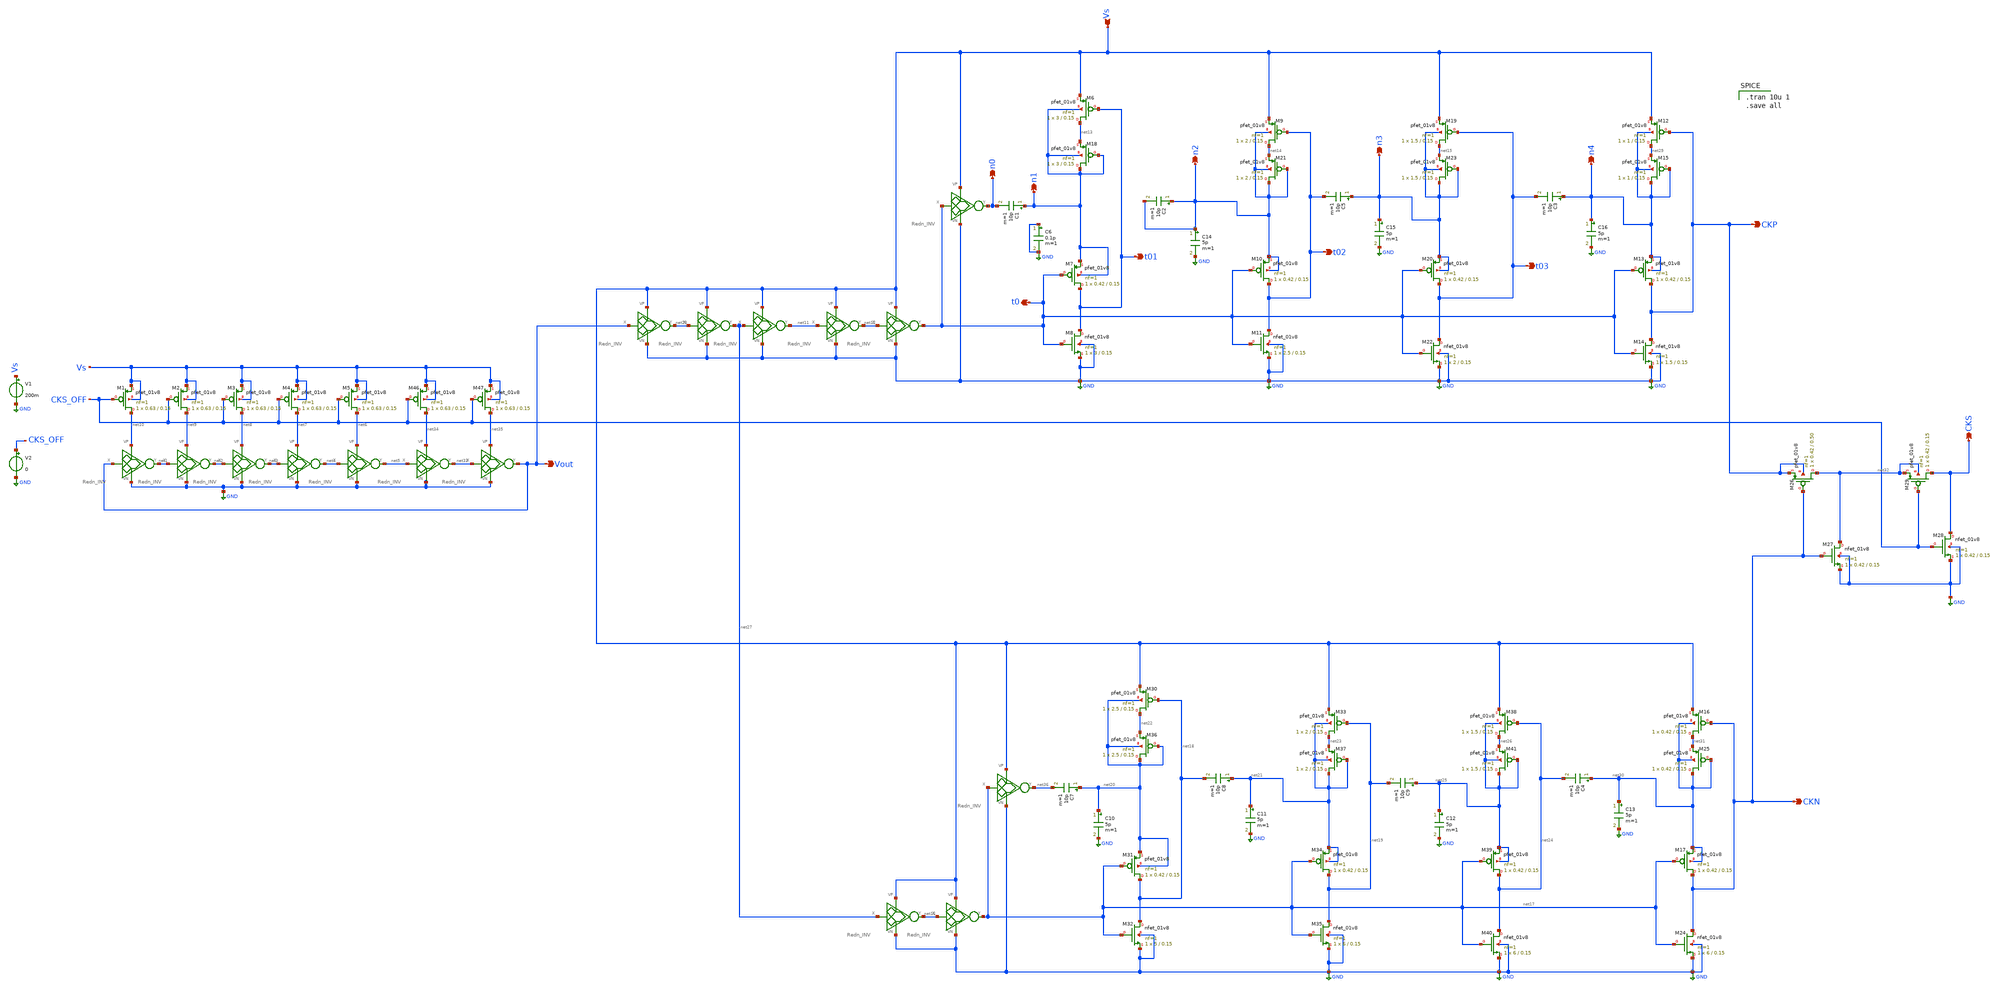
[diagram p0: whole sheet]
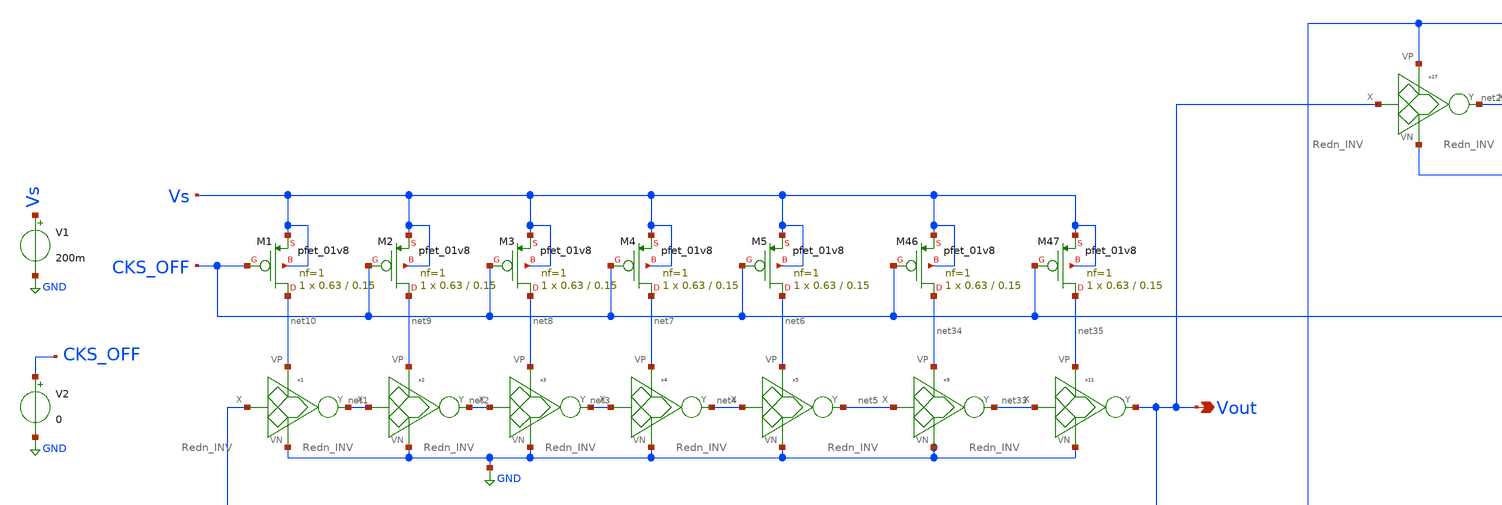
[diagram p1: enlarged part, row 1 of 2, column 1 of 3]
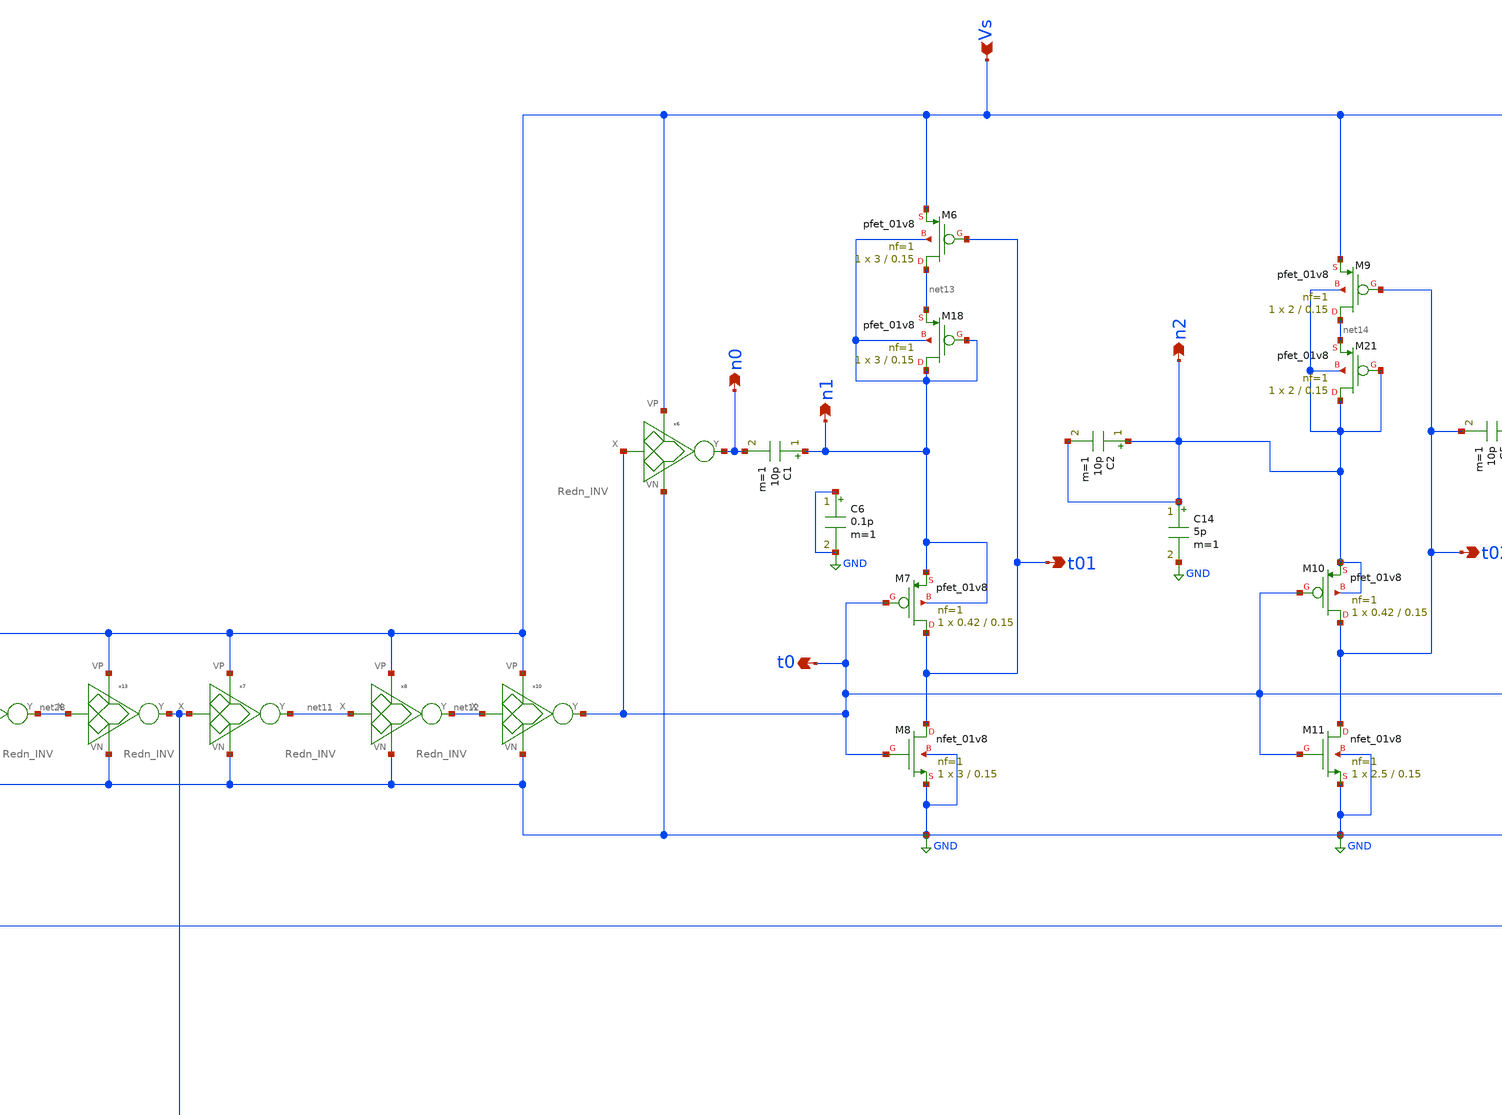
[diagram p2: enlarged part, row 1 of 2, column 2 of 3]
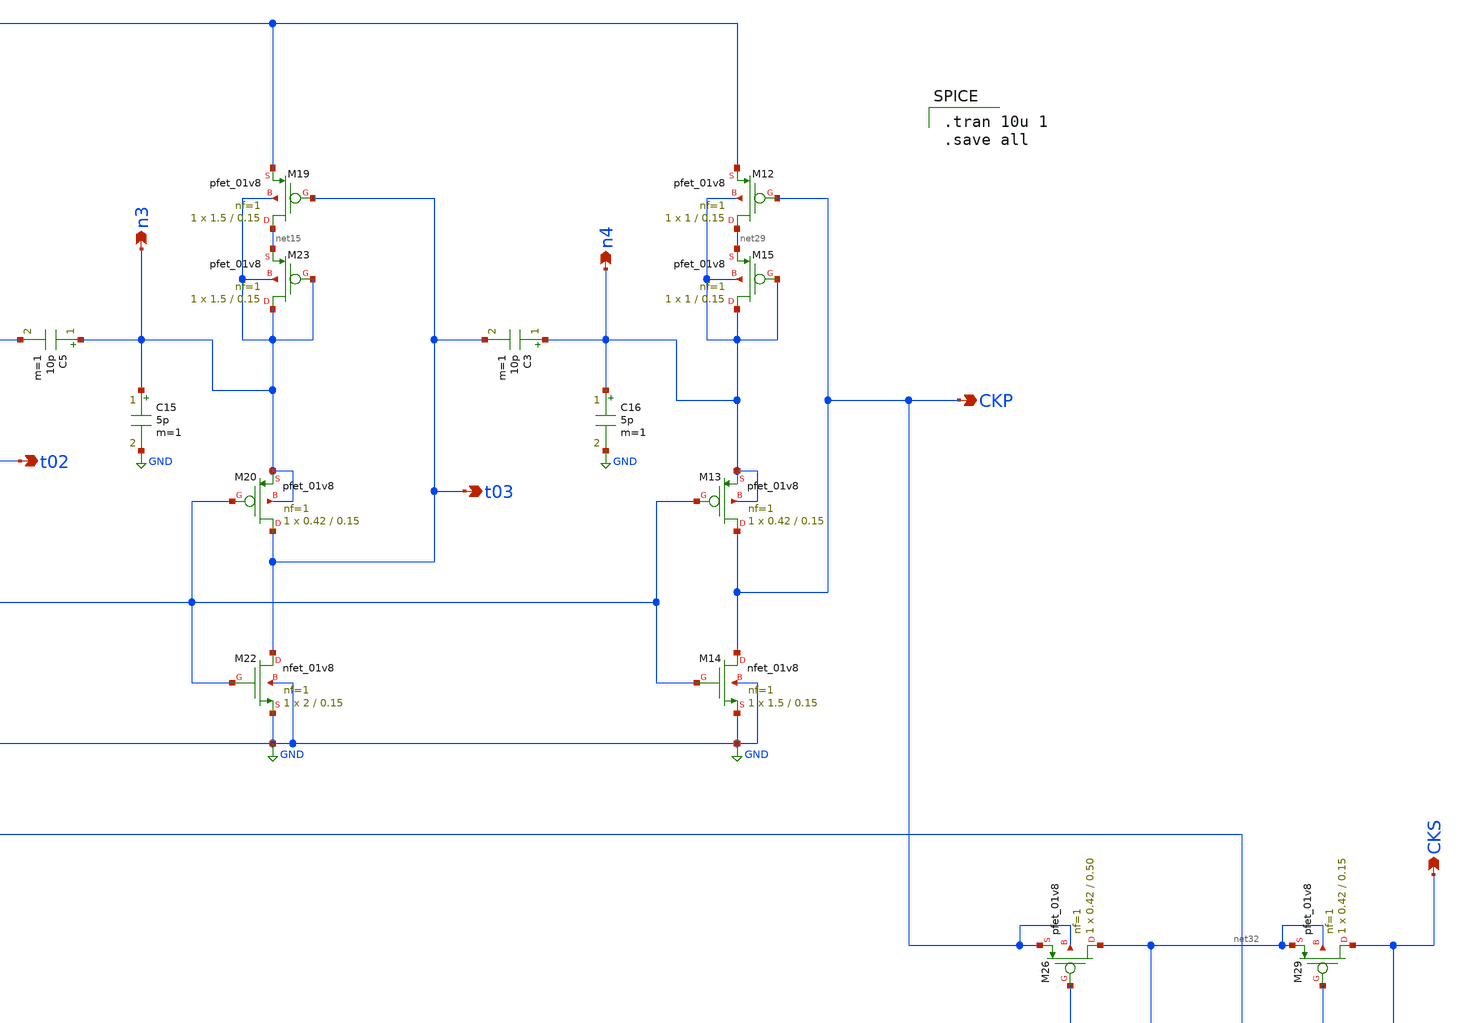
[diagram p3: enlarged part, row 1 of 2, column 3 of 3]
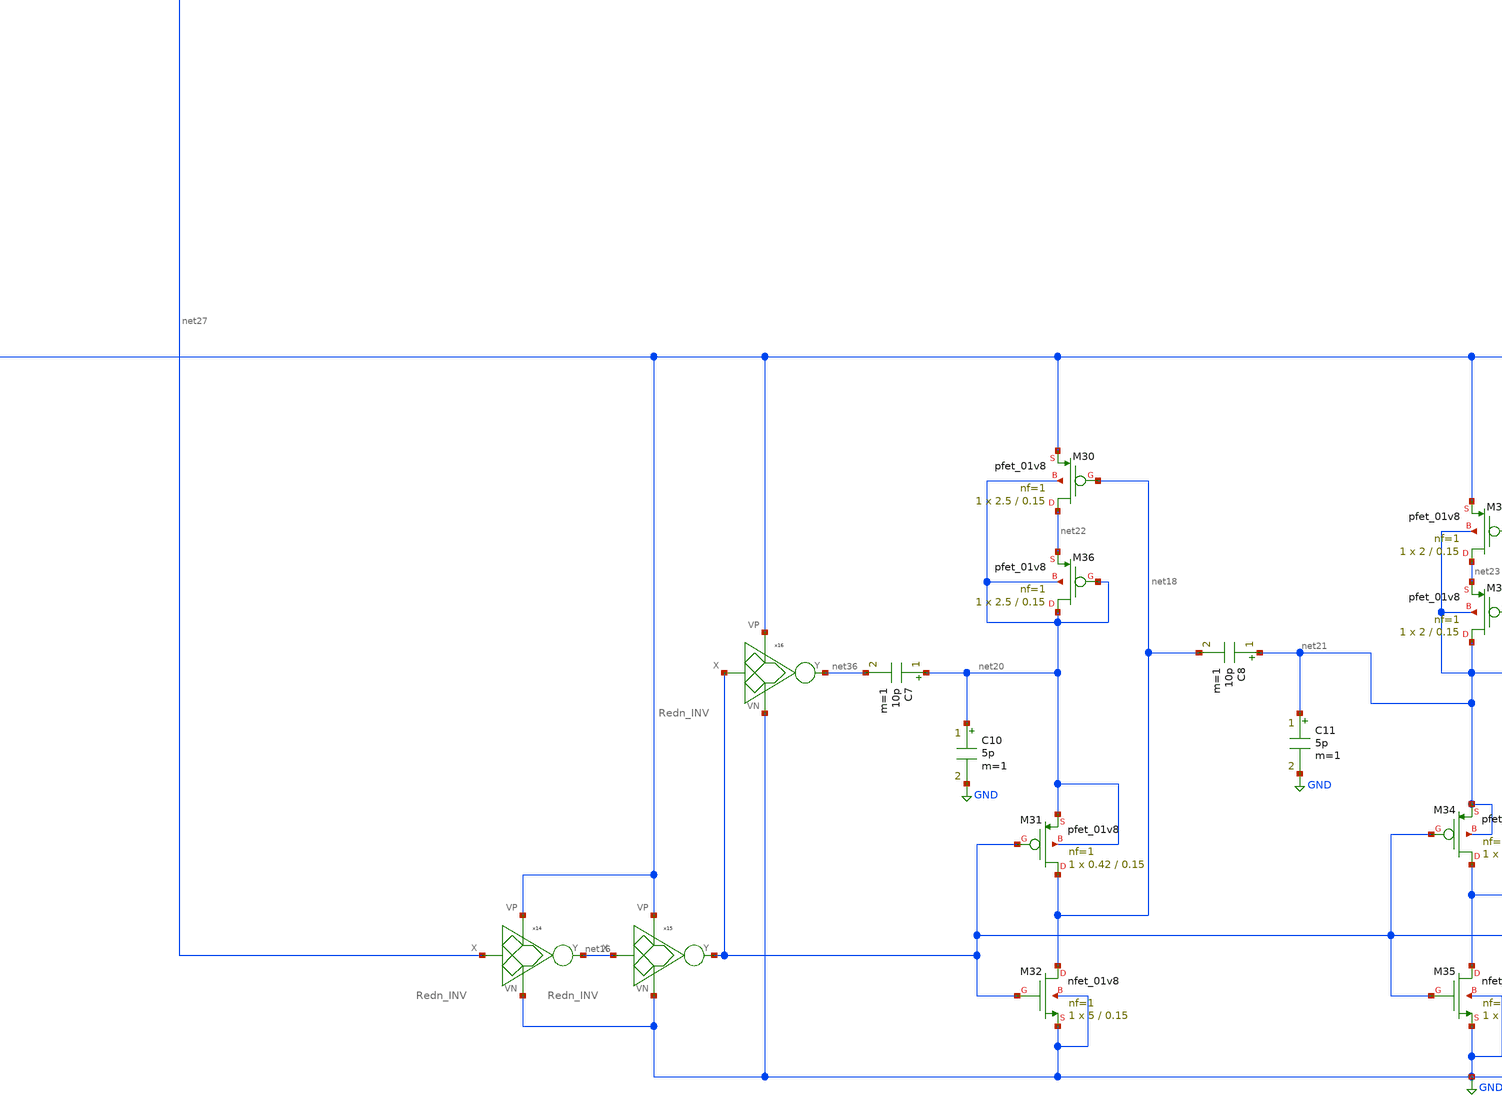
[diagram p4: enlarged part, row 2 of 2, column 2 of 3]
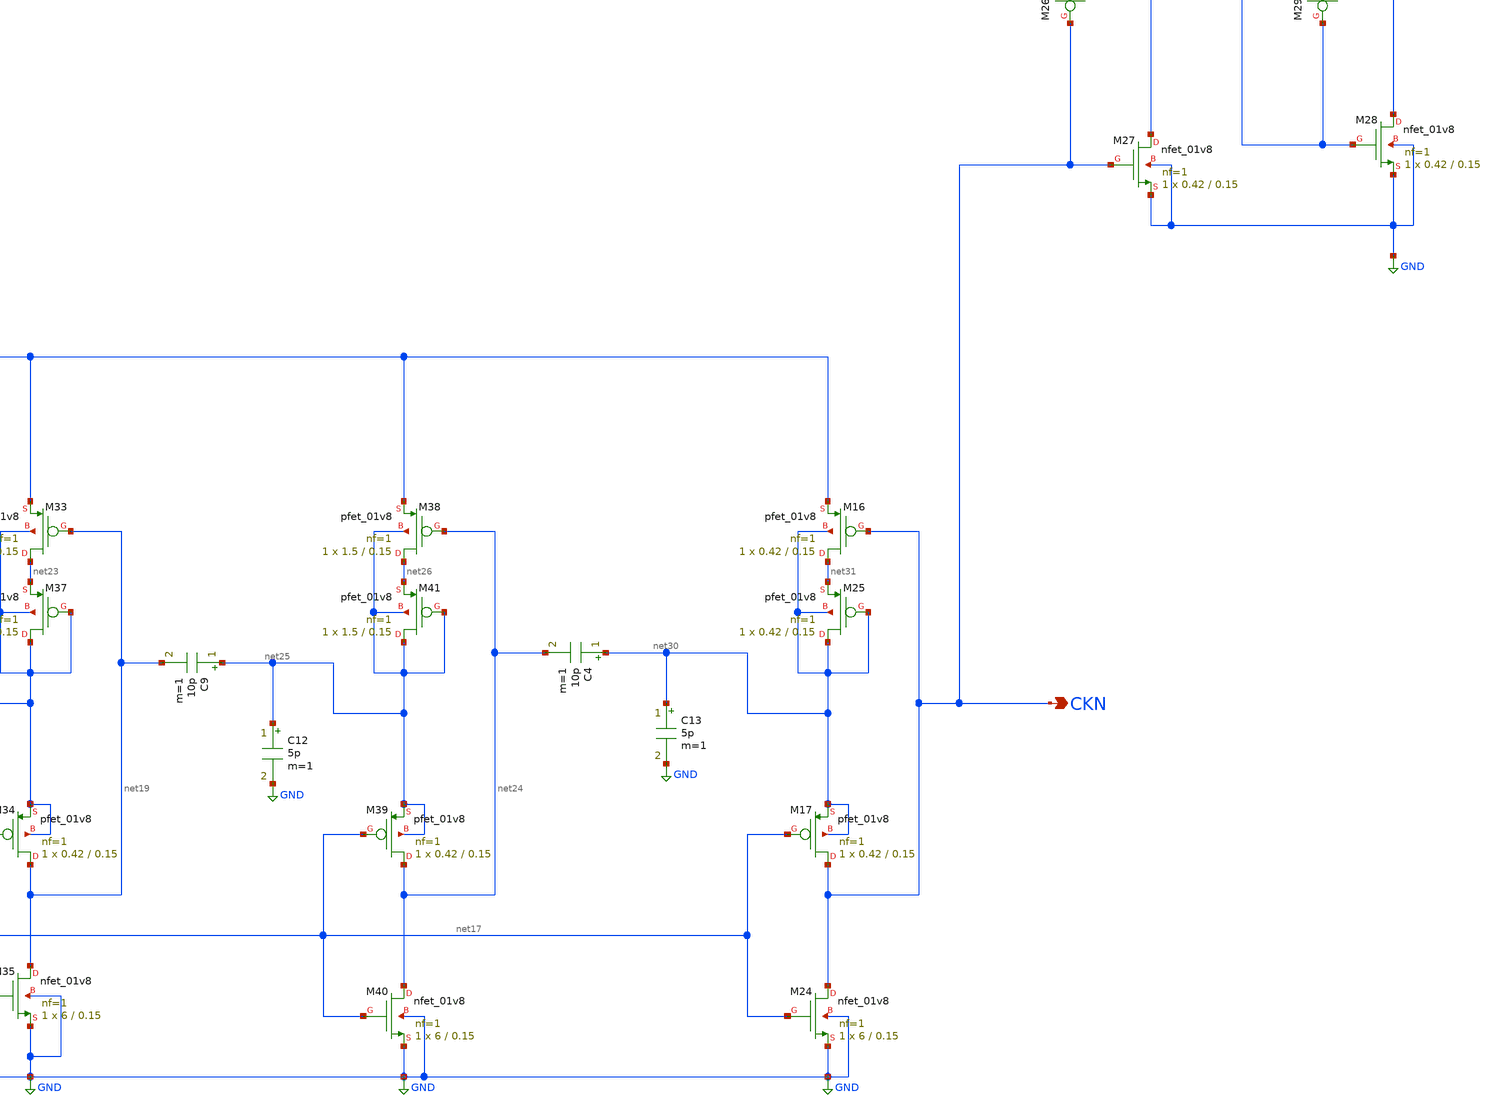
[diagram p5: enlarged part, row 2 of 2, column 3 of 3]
** sch_path: Blocks/Startup Converter/Startup_Conv_3.sch
**.subckt Startup_Conv_3 Vout Vs t02 CKP CKN CKS t03 t01 t0 n1 n2 n3 n4 n0
*.opin Vout
*.ipin Vs
*.opin t02
*.opin CKP
*.opin CKN
*.opin CKS
*.opin t03
*.opin t01
*.opin t0
*.opin n1
*.opin n2
*.opin n3
*.opin n4
*.opin n0
V1 Vs GND 200m
XM1 net10 CKS_OFF Vs Vs sky130_fd_pr__pfet_01v8 L=0.15 W=0.63 nf=1 ad='int((nf+1)/2) * W/nf * 0.29' as='int((nf+2)/2) * W/nf * 0.29'
+ pd='2*int((nf+1)/2) * (W/nf + 0.29)' ps='2*int((nf+2)/2) * (W/nf + 0.29)' nrd='0.29 / W' nrs='0.29 / W'
+ sa=0 sb=0 sd=0 mult=1 m=1
XM2 net9 CKS_OFF Vs Vs sky130_fd_pr__pfet_01v8 L=0.15 W=0.63 nf=1 ad='int((nf+1)/2) * W/nf * 0.29' as='int((nf+2)/2) * W/nf * 0.29'
+ pd='2*int((nf+1)/2) * (W/nf + 0.29)' ps='2*int((nf+2)/2) * (W/nf + 0.29)' nrd='0.29 / W' nrs='0.29 / W'
+ sa=0 sb=0 sd=0 mult=1 m=1
XM3 net8 CKS_OFF Vs Vs sky130_fd_pr__pfet_01v8 L=0.15 W=0.63 nf=1 ad='int((nf+1)/2) * W/nf * 0.29' as='int((nf+2)/2) * W/nf * 0.29'
+ pd='2*int((nf+1)/2) * (W/nf + 0.29)' ps='2*int((nf+2)/2) * (W/nf + 0.29)' nrd='0.29 / W' nrs='0.29 / W'
+ sa=0 sb=0 sd=0 mult=1 m=1
XM4 net7 CKS_OFF Vs Vs sky130_fd_pr__pfet_01v8 L=0.15 W=0.63 nf=1 ad='int((nf+1)/2) * W/nf * 0.29' as='int((nf+2)/2) * W/nf * 0.29'
+ pd='2*int((nf+1)/2) * (W/nf + 0.29)' ps='2*int((nf+2)/2) * (W/nf + 0.29)' nrd='0.29 / W' nrs='0.29 / W'
+ sa=0 sb=0 sd=0 mult=1 m=1
XM5 net6 CKS_OFF Vs Vs sky130_fd_pr__pfet_01v8 L=0.15 W=0.63 nf=1 ad='int((nf+1)/2) * W/nf * 0.29' as='int((nf+2)/2) * W/nf * 0.29'
+ pd='2*int((nf+1)/2) * (W/nf + 0.29)' ps='2*int((nf+2)/2) * (W/nf + 0.29)' nrd='0.29 / W' nrs='0.29 / W'
+ sa=0 sb=0 sd=0 mult=1 m=1
V2 CKS_OFF GND 0
x1 Vout net1 net10 GND Redn_INV
x2 net1 net2 net9 GND Redn_INV
x3 net2 net3 net8 GND Redn_INV
x4 net3 net4 net7 GND Redn_INV
x5 net4 net5 net6 GND Redn_INV
C1 n1 n0 10p m=1
XM6 net13 t01 Vs n1 sky130_fd_pr__pfet_01v8 L=0.15 W=3 nf=1 ad='int((nf+1)/2) * W/nf * 0.29' as='int((nf+2)/2) * W/nf * 0.29'
+ pd='2*int((nf+1)/2) * (W/nf + 0.29)' ps='2*int((nf+2)/2) * (W/nf + 0.29)' nrd='0.29 / W' nrs='0.29 / W'
+ sa=0 sb=0 sd=0 mult=1 m=1
XM9 net14 t02 Vs n2 sky130_fd_pr__pfet_01v8 L=0.15 W=2 nf=1 ad='int((nf+1)/2) * W/nf * 0.29' as='int((nf+2)/2) * W/nf * 0.29'
+ pd='2*int((nf+1)/2) * (W/nf + 0.29)' ps='2*int((nf+2)/2) * (W/nf + 0.29)' nrd='0.29 / W' nrs='0.29 / W'
+ sa=0 sb=0 sd=0 mult=1 m=1
XM10 t02 t0 n2 n2 sky130_fd_pr__pfet_01v8 L=0.15 W=0.42 nf=1 ad='int((nf+1)/2) * W/nf * 0.29' as='int((nf+2)/2) * W/nf * 0.29'
+ pd='2*int((nf+1)/2) * (W/nf + 0.29)' ps='2*int((nf+2)/2) * (W/nf + 0.29)' nrd='0.29 / W' nrs='0.29 / W'
+ sa=0 sb=0 sd=0 mult=1 m=1
XM11 t02 t0 GND GND sky130_fd_pr__nfet_01v8 L=0.15 W=2.5 nf=1 ad='int((nf+1)/2) * W/nf * 0.29' as='int((nf+2)/2) * W/nf * 0.29'
+ pd='2*int((nf+1)/2) * (W/nf + 0.29)' ps='2*int((nf+2)/2) * (W/nf + 0.29)' nrd='0.29 / W' nrs='0.29 / W'
+ sa=0 sb=0 sd=0 mult=1 m=1
XM18 n1 n1 net13 n1 sky130_fd_pr__pfet_01v8 L=0.15 W=3 nf=1 ad='int((nf+1)/2) * W/nf * 0.29' as='int((nf+2)/2) * W/nf * 0.29'
+ pd='2*int((nf+1)/2) * (W/nf + 0.29)' ps='2*int((nf+2)/2) * (W/nf + 0.29)' nrd='0.29 / W' nrs='0.29 / W'
+ sa=0 sb=0 sd=0 mult=1 m=1
XM21 n2 n2 net14 n2 sky130_fd_pr__pfet_01v8 L=0.15 W=2 nf=1 ad='int((nf+1)/2) * W/nf * 0.29' as='int((nf+2)/2) * W/nf * 0.29'
+ pd='2*int((nf+1)/2) * (W/nf + 0.29)' ps='2*int((nf+2)/2) * (W/nf + 0.29)' nrd='0.29 / W' nrs='0.29 / W'
+ sa=0 sb=0 sd=0 mult=1 m=1
C2 n2 n2 10p m=1
x7 net27 net11 Vs GND Redn_INV
x8 net11 net12 Vs GND Redn_INV
x10 net12 t0 Vs GND Redn_INV
x6 t0 n0 Vs GND Redn_INV
XM19 net15 t03 Vs n3 sky130_fd_pr__pfet_01v8 L=0.15 W=1.5 nf=1 ad='int((nf+1)/2) * W/nf * 0.29' as='int((nf+2)/2) * W/nf * 0.29'
+ pd='2*int((nf+1)/2) * (W/nf + 0.29)' ps='2*int((nf+2)/2) * (W/nf + 0.29)' nrd='0.29 / W' nrs='0.29 / W'
+ sa=0 sb=0 sd=0 mult=1 m=1
XM20 t03 t0 n3 n3 sky130_fd_pr__pfet_01v8 L=0.15 W=0.42 nf=1 ad='int((nf+1)/2) * W/nf * 0.29' as='int((nf+2)/2) * W/nf * 0.29'
+ pd='2*int((nf+1)/2) * (W/nf + 0.29)' ps='2*int((nf+2)/2) * (W/nf + 0.29)' nrd='0.29 / W' nrs='0.29 / W'
+ sa=0 sb=0 sd=0 mult=1 m=1
XM22 t03 t0 GND GND sky130_fd_pr__nfet_01v8 L=0.15 W=2 nf=1 ad='int((nf+1)/2) * W/nf * 0.29' as='int((nf+2)/2) * W/nf * 0.29'
+ pd='2*int((nf+1)/2) * (W/nf + 0.29)' ps='2*int((nf+2)/2) * (W/nf + 0.29)' nrd='0.29 / W' nrs='0.29 / W'
+ sa=0 sb=0 sd=0 mult=1 m=1
XM23 n3 n3 net15 n3 sky130_fd_pr__pfet_01v8 L=0.15 W=1.5 nf=1 ad='int((nf+1)/2) * W/nf * 0.29' as='int((nf+2)/2) * W/nf * 0.29'
+ pd='2*int((nf+1)/2) * (W/nf + 0.29)' ps='2*int((nf+2)/2) * (W/nf + 0.29)' nrd='0.29 / W' nrs='0.29 / W'
+ sa=0 sb=0 sd=0 mult=1 m=1
C5 n3 t02 10p m=1
C7 net20 net36 10p m=1
XM30 net22 net18 Vs net20 sky130_fd_pr__pfet_01v8 L=0.15 W=2.5 nf=1 ad='int((nf+1)/2) * W/nf * 0.29'
+ as='int((nf+2)/2) * W/nf * 0.29' pd='2*int((nf+1)/2) * (W/nf + 0.29)' ps='2*int((nf+2)/2) * (W/nf + 0.29)'
+ nrd='0.29 / W' nrs='0.29 / W' sa=0 sb=0 sd=0 mult=1 m=1
XM31 net18 net17 net20 net20 sky130_fd_pr__pfet_01v8 L=0.15 W=0.42 nf=1 ad='int((nf+1)/2) * W/nf * 0.29'
+ as='int((nf+2)/2) * W/nf * 0.29' pd='2*int((nf+1)/2) * (W/nf + 0.29)' ps='2*int((nf+2)/2) * (W/nf + 0.29)'
+ nrd='0.29 / W' nrs='0.29 / W' sa=0 sb=0 sd=0 mult=1 m=1
XM32 net18 net17 GND GND sky130_fd_pr__nfet_01v8 L=0.15 W=5 nf=1 ad='int((nf+1)/2) * W/nf * 0.29' as='int((nf+2)/2) * W/nf * 0.29'
+ pd='2*int((nf+1)/2) * (W/nf + 0.29)' ps='2*int((nf+2)/2) * (W/nf + 0.29)' nrd='0.29 / W' nrs='0.29 / W'
+ sa=0 sb=0 sd=0 mult=1 m=1
XM33 net23 net19 Vs net21 sky130_fd_pr__pfet_01v8 L=0.15 W=2 nf=1 ad='int((nf+1)/2) * W/nf * 0.29' as='int((nf+2)/2) * W/nf * 0.29'
+ pd='2*int((nf+1)/2) * (W/nf + 0.29)' ps='2*int((nf+2)/2) * (W/nf + 0.29)' nrd='0.29 / W' nrs='0.29 / W'
+ sa=0 sb=0 sd=0 mult=1 m=1
XM34 net19 net17 net21 net21 sky130_fd_pr__pfet_01v8 L=0.15 W=0.42 nf=1 ad='int((nf+1)/2) * W/nf * 0.29'
+ as='int((nf+2)/2) * W/nf * 0.29' pd='2*int((nf+1)/2) * (W/nf + 0.29)' ps='2*int((nf+2)/2) * (W/nf + 0.29)'
+ nrd='0.29 / W' nrs='0.29 / W' sa=0 sb=0 sd=0 mult=1 m=1
XM35 net19 net17 GND GND sky130_fd_pr__nfet_01v8 L=0.15 W=6 nf=1 ad='int((nf+1)/2) * W/nf * 0.29' as='int((nf+2)/2) * W/nf * 0.29'
+ pd='2*int((nf+1)/2) * (W/nf + 0.29)' ps='2*int((nf+2)/2) * (W/nf + 0.29)' nrd='0.29 / W' nrs='0.29 / W'
+ sa=0 sb=0 sd=0 mult=1 m=1
XM36 net20 net20 net22 net20 sky130_fd_pr__pfet_01v8 L=0.15 W=2.5 nf=1 ad='int((nf+1)/2) * W/nf * 0.29'
+ as='int((nf+2)/2) * W/nf * 0.29' pd='2*int((nf+1)/2) * (W/nf + 0.29)' ps='2*int((nf+2)/2) * (W/nf + 0.29)'
+ nrd='0.29 / W' nrs='0.29 / W' sa=0 sb=0 sd=0 mult=1 m=1
XM37 net21 net21 net23 net21 sky130_fd_pr__pfet_01v8 L=0.15 W=2 nf=1 ad='int((nf+1)/2) * W/nf * 0.29'
+ as='int((nf+2)/2) * W/nf * 0.29' pd='2*int((nf+1)/2) * (W/nf + 0.29)' ps='2*int((nf+2)/2) * (W/nf + 0.29)'
+ nrd='0.29 / W' nrs='0.29 / W' sa=0 sb=0 sd=0 mult=1 m=1
C8 net21 net18 10p m=1
x14 net27 net16 Vs GND Redn_INV
x15 net16 net17 Vs GND Redn_INV
x16 net17 net36 Vs GND Redn_INV
XM38 net26 net24 Vs net25 sky130_fd_pr__pfet_01v8 L=0.15 W=1.5 nf=1 ad='int((nf+1)/2) * W/nf * 0.29'
+ as='int((nf+2)/2) * W/nf * 0.29' pd='2*int((nf+1)/2) * (W/nf + 0.29)' ps='2*int((nf+2)/2) * (W/nf + 0.29)'
+ nrd='0.29 / W' nrs='0.29 / W' sa=0 sb=0 sd=0 mult=1 m=1
XM39 net24 net17 net25 net25 sky130_fd_pr__pfet_01v8 L=0.15 W=0.42 nf=1 ad='int((nf+1)/2) * W/nf * 0.29'
+ as='int((nf+2)/2) * W/nf * 0.29' pd='2*int((nf+1)/2) * (W/nf + 0.29)' ps='2*int((nf+2)/2) * (W/nf + 0.29)'
+ nrd='0.29 / W' nrs='0.29 / W' sa=0 sb=0 sd=0 mult=1 m=1
XM40 net24 net17 GND GND sky130_fd_pr__nfet_01v8 L=0.15 W=6 nf=1 ad='int((nf+1)/2) * W/nf * 0.29' as='int((nf+2)/2) * W/nf * 0.29'
+ pd='2*int((nf+1)/2) * (W/nf + 0.29)' ps='2*int((nf+2)/2) * (W/nf + 0.29)' nrd='0.29 / W' nrs='0.29 / W'
+ sa=0 sb=0 sd=0 mult=1 m=1
XM41 net25 net25 net26 net25 sky130_fd_pr__pfet_01v8 L=0.15 W=1.5 nf=1 ad='int((nf+1)/2) * W/nf * 0.29'
+ as='int((nf+2)/2) * W/nf * 0.29' pd='2*int((nf+1)/2) * (W/nf + 0.29)' ps='2*int((nf+2)/2) * (W/nf + 0.29)'
+ nrd='0.29 / W' nrs='0.29 / W' sa=0 sb=0 sd=0 mult=1 m=1
C9 net25 net19 10p m=1
x13 net28 net27 Vs GND Redn_INV
x17 Vout net28 Vs GND Redn_INV
XM12 net29 CKP Vs n4 sky130_fd_pr__pfet_01v8 L=0.15 W=1 nf=1 ad='int((nf+1)/2) * W/nf * 0.29' as='int((nf+2)/2) * W/nf * 0.29'
+ pd='2*int((nf+1)/2) * (W/nf + 0.29)' ps='2*int((nf+2)/2) * (W/nf + 0.29)' nrd='0.29 / W' nrs='0.29 / W'
+ sa=0 sb=0 sd=0 mult=1 m=1
XM13 CKP t0 n4 n4 sky130_fd_pr__pfet_01v8 L=0.15 W=0.42 nf=1 ad='int((nf+1)/2) * W/nf * 0.29' as='int((nf+2)/2) * W/nf * 0.29'
+ pd='2*int((nf+1)/2) * (W/nf + 0.29)' ps='2*int((nf+2)/2) * (W/nf + 0.29)' nrd='0.29 / W' nrs='0.29 / W'
+ sa=0 sb=0 sd=0 mult=1 m=1
XM14 CKP t0 GND GND sky130_fd_pr__nfet_01v8 L=0.15 W=1.5 nf=1 ad='int((nf+1)/2) * W/nf * 0.29' as='int((nf+2)/2) * W/nf * 0.29'
+ pd='2*int((nf+1)/2) * (W/nf + 0.29)' ps='2*int((nf+2)/2) * (W/nf + 0.29)' nrd='0.29 / W' nrs='0.29 / W'
+ sa=0 sb=0 sd=0 mult=1 m=1
XM15 n4 n4 net29 n4 sky130_fd_pr__pfet_01v8 L=0.15 W=1 nf=1 ad='int((nf+1)/2) * W/nf * 0.29' as='int((nf+2)/2) * W/nf * 0.29'
+ pd='2*int((nf+1)/2) * (W/nf + 0.29)' ps='2*int((nf+2)/2) * (W/nf + 0.29)' nrd='0.29 / W' nrs='0.29 / W'
+ sa=0 sb=0 sd=0 mult=1 m=1
C3 n4 t03 10p m=1
XM16 net31 CKN Vs net30 sky130_fd_pr__pfet_01v8 L=0.15 W=0.42 nf=1 ad='int((nf+1)/2) * W/nf * 0.29' as='int((nf+2)/2) * W/nf * 0.29'
+ pd='2*int((nf+1)/2) * (W/nf + 0.29)' ps='2*int((nf+2)/2) * (W/nf + 0.29)' nrd='0.29 / W' nrs='0.29 / W'
+ sa=0 sb=0 sd=0 mult=1 m=1
XM17 CKN net17 net30 net30 sky130_fd_pr__pfet_01v8 L=0.15 W=0.42 nf=1 ad='int((nf+1)/2) * W/nf * 0.29'
+ as='int((nf+2)/2) * W/nf * 0.29' pd='2*int((nf+1)/2) * (W/nf + 0.29)' ps='2*int((nf+2)/2) * (W/nf + 0.29)'
+ nrd='0.29 / W' nrs='0.29 / W' sa=0 sb=0 sd=0 mult=1 m=1
XM24 CKN net17 GND GND sky130_fd_pr__nfet_01v8 L=0.15 W=6 nf=1 ad='int((nf+1)/2) * W/nf * 0.29' as='int((nf+2)/2) * W/nf * 0.29'
+ pd='2*int((nf+1)/2) * (W/nf + 0.29)' ps='2*int((nf+2)/2) * (W/nf + 0.29)' nrd='0.29 / W' nrs='0.29 / W'
+ sa=0 sb=0 sd=0 mult=1 m=1
XM25 net30 net30 net31 net30 sky130_fd_pr__pfet_01v8 L=0.15 W=0.42 nf=1 ad='int((nf+1)/2) * W/nf * 0.29'
+ as='int((nf+2)/2) * W/nf * 0.29' pd='2*int((nf+1)/2) * (W/nf + 0.29)' ps='2*int((nf+2)/2) * (W/nf + 0.29)'
+ nrd='0.29 / W' nrs='0.29 / W' sa=0 sb=0 sd=0 mult=1 m=1
C4 net30 net24 10p m=1
XM26 net32 CKN CKP CKP sky130_fd_pr__pfet_01v8 L=0.50 W=0.42 nf=1 ad='int((nf+1)/2) * W/nf * 0.29' as='int((nf+2)/2) * W/nf * 0.29'
+ pd='2*int((nf+1)/2) * (W/nf + 0.29)' ps='2*int((nf+2)/2) * (W/nf + 0.29)' nrd='0.29 / W' nrs='0.29 / W'
+ sa=0 sb=0 sd=0 mult=1 m=1
XM27 net32 CKN GND GND sky130_fd_pr__nfet_01v8 L=0.15 W=0.42 nf=1 ad='int((nf+1)/2) * W/nf * 0.29' as='int((nf+2)/2) * W/nf * 0.29'
+ pd='2*int((nf+1)/2) * (W/nf + 0.29)' ps='2*int((nf+2)/2) * (W/nf + 0.29)' nrd='0.29 / W' nrs='0.29 / W'
+ sa=0 sb=0 sd=0 mult=1 m=1
XM28 CKS CKS_OFF GND GND sky130_fd_pr__nfet_01v8 L=0.15 W=0.42 nf=1 ad='int((nf+1)/2) * W/nf * 0.29'
+ as='int((nf+2)/2) * W/nf * 0.29' pd='2*int((nf+1)/2) * (W/nf + 0.29)' ps='2*int((nf+2)/2) * (W/nf + 0.29)'
+ nrd='0.29 / W' nrs='0.29 / W' sa=0 sb=0 sd=0 mult=1 m=1
XM29 CKS CKS_OFF net32 net32 sky130_fd_pr__pfet_01v8 L=0.15 W=0.42 nf=1 ad='int((nf+1)/2) * W/nf * 0.29'
+ as='int((nf+2)/2) * W/nf * 0.29' pd='2*int((nf+1)/2) * (W/nf + 0.29)' ps='2*int((nf+2)/2) * (W/nf + 0.29)'
+ nrd='0.29 / W' nrs='0.29 / W' sa=0 sb=0 sd=0 mult=1 m=1
x9 net5 net33 net34 GND Redn_INV
x11 net33 Vout net35 GND Redn_INV
XM46 net34 CKS_OFF Vs Vs sky130_fd_pr__pfet_01v8 L=0.15 W=0.63 nf=1 ad='int((nf+1)/2) * W/nf * 0.29'
+ as='int((nf+2)/2) * W/nf * 0.29' pd='2*int((nf+1)/2) * (W/nf + 0.29)' ps='2*int((nf+2)/2) * (W/nf + 0.29)'
+ nrd='0.29 / W' nrs='0.29 / W' sa=0 sb=0 sd=0 mult=1 m=1
XM47 net35 CKS_OFF Vs Vs sky130_fd_pr__pfet_01v8 L=0.15 W=0.63 nf=1 ad='int((nf+1)/2) * W/nf * 0.29'
+ as='int((nf+2)/2) * W/nf * 0.29' pd='2*int((nf+1)/2) * (W/nf + 0.29)' ps='2*int((nf+2)/2) * (W/nf + 0.29)'
+ nrd='0.29 / W' nrs='0.29 / W' sa=0 sb=0 sd=0 mult=1 m=1
C11 net21 GND 5p m=1
C12 net25 GND 5p m=1
C13 net30 GND 5p m=1
C14 n2 GND 5p m=1
C15 n3 GND 5p m=1
C16 n4 GND 5p m=1
C6 GND GND 0.1p m=1
C10 net20 GND 5p m=1
XM7 t01 t0 n1 n1 sky130_fd_pr__pfet_01v8 L=0.15 W=0.42 nf=1 ad='int((nf+1)/2) * W/nf * 0.29' as='int((nf+2)/2) * W/nf * 0.29'
+ pd='2*int((nf+1)/2) * (W/nf + 0.29)' ps='2*int((nf+2)/2) * (W/nf + 0.29)' nrd='0.29 / W' nrs='0.29 / W'
+ sa=0 sb=0 sd=0 mult=1 m=1
XM8 t01 t0 GND GND sky130_fd_pr__nfet_01v8 L=0.15 W=3 nf=1 ad='int((nf+1)/2) * W/nf * 0.29' as='int((nf+2)/2) * W/nf * 0.29'
+ pd='2*int((nf+1)/2) * (W/nf + 0.29)' ps='2*int((nf+2)/2) * (W/nf + 0.29)' nrd='0.29 / W' nrs='0.29 / W'
+ sa=0 sb=0 sd=0 mult=1 m=1
**** begin user architecture code

** opencircuitdesign pdks install
.lib $::SKYWATER_MODELS/sky130.lib.spice tt



.tran 10u 1
.save all

**** end user architecture code
**.ends

* expanding   symbol:  component/Reduntant_Inverter/Redn_INV.sym # of pins=4
** sym_path: component/Reduntant_Inverter/Redn_INV.sym
** sch_path: component/Reduntant_Inverter/Redn_INV.sch
.subckt Redn_INV X Y VP VN
*.opin Y
*.ipin X
*.iopin VP
*.iopin VN
XM15 net4 X VN VN sky130_fd_pr__nfet_01v8_lvt L=0.15 W=1 nf=1 ad='int((nf+1)/2) * W/nf * 0.29' as='int((nf+2)/2) * W/nf * 0.29'
+ pd='2*int((nf+1)/2) * (W/nf + 0.29)' ps='2*int((nf+2)/2) * (W/nf + 0.29)' nrd='0.29 / W' nrs='0.29 / W'
+ sa=0 sb=0 sd=0 mult=1 m=1
XM1 net5 X net3 VN sky130_fd_pr__nfet_01v8_lvt L=0.15 W=3.25 nf=1 ad='int((nf+1)/2) * W/nf * 0.29' as='int((nf+2)/2) * W/nf * 0.29'
+ pd='2*int((nf+1)/2) * (W/nf + 0.29)' ps='2*int((nf+2)/2) * (W/nf + 0.29)' nrd='0.29 / W' nrs='0.29 / W'
+ sa=0 sb=0 sd=0 mult=1 m=1
XM16 Y X net6 VN sky130_fd_pr__nfet_01v8_lvt L=0.15 W=6.5 nf=1 ad='int((nf+1)/2) * W/nf * 0.29' as='int((nf+2)/2) * W/nf * 0.29'
+ pd='2*int((nf+1)/2) * (W/nf + 0.29)' ps='2*int((nf+2)/2) * (W/nf + 0.29)' nrd='0.29 / W' nrs='0.29 / W'
+ sa=0 sb=0 sd=0 mult=1 m=1
XM17 net3 X VN VN sky130_fd_pr__nfet_01v8_lvt L=0.15 W=3.25 nf=1 ad='int((nf+1)/2) * W/nf * 0.29' as='int((nf+2)/2) * W/nf * 0.29'
+ pd='2*int((nf+1)/2) * (W/nf + 0.29)' ps='2*int((nf+2)/2) * (W/nf + 0.29)' nrd='0.29 / W' nrs='0.29 / W'
+ sa=0 sb=0 sd=0 mult=1 m=1
XM18 net2 X VN VN sky130_fd_pr__nfet_01v8_lvt L=0.15 W=1.5 nf=1 ad='int((nf+1)/2) * W/nf * 0.29' as='int((nf+2)/2) * W/nf * 0.29'
+ pd='2*int((nf+1)/2) * (W/nf + 0.29)' ps='2*int((nf+2)/2) * (W/nf + 0.29)' nrd='0.29 / W' nrs='0.29 / W'
+ sa=0 sb=0 sd=0 mult=1 m=1
XM19 net1 X VN VN sky130_fd_pr__nfet_01v8_lvt L=0.15 W=6.5 nf=1 ad='int((nf+1)/2) * W/nf * 0.29' as='int((nf+2)/2) * W/nf * 0.29'
+ pd='2*int((nf+1)/2) * (W/nf + 0.29)' ps='2*int((nf+2)/2) * (W/nf + 0.29)' nrd='0.29 / W' nrs='0.29 / W'
+ sa=0 sb=0 sd=0 mult=1 m=1
XM20 net6 X net1 VN sky130_fd_pr__nfet_01v8_lvt L=0.15 W=6.5 nf=1 ad='int((nf+1)/2) * W/nf * 0.29' as='int((nf+2)/2) * W/nf * 0.29'
+ pd='2*int((nf+1)/2) * (W/nf + 0.29)' ps='2*int((nf+2)/2) * (W/nf + 0.29)' nrd='0.29 / W' nrs='0.29 / W'
+ sa=0 sb=0 sd=0 mult=1 m=1
XM2 net4 X VP VP sky130_fd_pr__pfet_01v8 L=0.15 W=10 nf=1 ad='int((nf+1)/2) * W/nf * 0.29' as='int((nf+2)/2) * W/nf * 0.29'
+ pd='2*int((nf+1)/2) * (W/nf + 0.29)' ps='2*int((nf+2)/2) * (W/nf + 0.29)' nrd='0.29 / W' nrs='0.29 / W'
+ sa=0 sb=0 sd=0 mult=1 m=1
XM5 net5 X net4 net4 sky130_fd_pr__pfet_01v8 L=0.15 W=10 nf=1 ad='int((nf+1)/2) * W/nf * 0.29' as='int((nf+2)/2) * W/nf * 0.29'
+ pd='2*int((nf+1)/2) * (W/nf + 0.29)' ps='2*int((nf+2)/2) * (W/nf + 0.29)' nrd='0.29 / W' nrs='0.29 / W'
+ sa=0 sb=0 sd=0 mult=1 m=1
XM6 Y X net5 VP sky130_fd_pr__pfet_01v8 L=0.15 W=10 nf=1 ad='int((nf+1)/2) * W/nf * 0.29' as='int((nf+2)/2) * W/nf * 0.29'
+ pd='2*int((nf+1)/2) * (W/nf + 0.29)' ps='2*int((nf+2)/2) * (W/nf + 0.29)' nrd='0.29 / W' nrs='0.29 / W'
+ sa=0 sb=0 sd=0 mult=1 m=1
XM8 net3 X VP VP sky130_fd_pr__pfet_01v8 L=0.15 W=2 nf=1 ad='int((nf+1)/2) * W/nf * 0.29' as='int((nf+2)/2) * W/nf * 0.29'
+ pd='2*int((nf+1)/2) * (W/nf + 0.29)' ps='2*int((nf+2)/2) * (W/nf + 0.29)' nrd='0.29 / W' nrs='0.29 / W'
+ sa=0 sb=0 sd=0 mult=1 m=1
XM12 net2 X VP VP sky130_fd_pr__pfet_01v8 L=0.15 W=5 nf=1 ad='int((nf+1)/2) * W/nf * 0.29' as='int((nf+2)/2) * W/nf * 0.29'
+ pd='2*int((nf+1)/2) * (W/nf + 0.29)' ps='2*int((nf+2)/2) * (W/nf + 0.29)' nrd='0.29 / W' nrs='0.29 / W'
+ sa=0 sb=0 sd=0 mult=1 m=1
XM14 net6 X net2 VP sky130_fd_pr__pfet_01v8 L=0.15 W=5 nf=1 ad='int((nf+1)/2) * W/nf * 0.29' as='int((nf+2)/2) * W/nf * 0.29'
+ pd='2*int((nf+1)/2) * (W/nf + 0.29)' ps='2*int((nf+2)/2) * (W/nf + 0.29)' nrd='0.29 / W' nrs='0.29 / W'
+ sa=0 sb=0 sd=0 mult=1 m=1
XM21 net1 X VP VP sky130_fd_pr__pfet_01v8 L=0.15 W=1.5 nf=1 ad='int((nf+1)/2) * W/nf * 0.29' as='int((nf+2)/2) * W/nf * 0.29'
+ pd='2*int((nf+1)/2) * (W/nf + 0.29)' ps='2*int((nf+2)/2) * (W/nf + 0.29)' nrd='0.29 / W' nrs='0.29 / W'
+ sa=0 sb=0 sd=0 mult=1 m=1
.ends

.GLOBAL GND
.end
